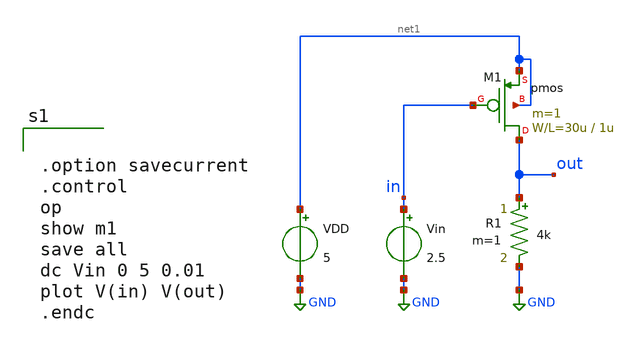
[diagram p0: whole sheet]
** sch_path: member_project/GroupWork/Team_masahiro/pfet_common_source_DC.sch
**.subckt pfet_common_source_DC
R1 out GND 4k m=1
VDD net1 GND 5
Vin in GND 2.5
M1 out in net1 net1 pmos L=1u W=30u m=1
**** begin user architecture code
 .include $::LIB/mos.lib
.include $::LIB/passive.lib
.include $::LIB/diode.lib


.option savecurrent
.control
op
show m1
save all
dc Vin 0 5 0.01
plot V(in) V(out)
.endc


**** end user architecture code
**.ends
.GLOBAL GND
.end
